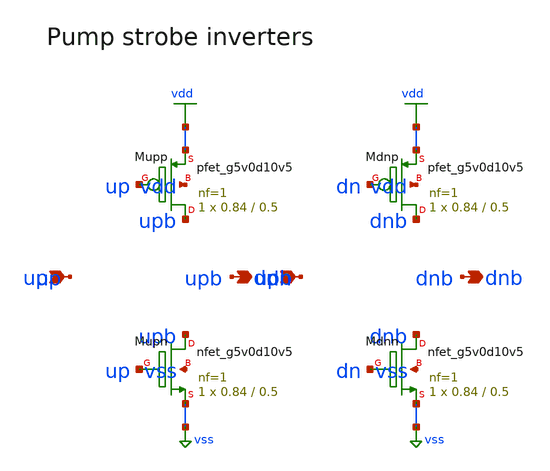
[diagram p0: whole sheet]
** sch_path: xschem/rt5w_pumpinv.sch
**.subckt rt5w_pumpinv up dn upb dnb
*.ipin up
*.ipin dn
*.opin upb
*.opin dnb
XMupp upb up vdd vdd sky130_fd_pr__pfet_g5v0d10v5 L=0.5 W=0.84 nf=1 ad=0.2436 as=0.2436 pd=2.26
+ ps=2.26 nrd=0.3452 nrs=0.3452 sa=0 sb=0 sd=0 mult=1 m=1
XMupn upb up vss vss sky130_fd_pr__nfet_g5v0d10v5 L=0.5 W=0.84 nf=1 ad=0.2436 as=0.2436 pd=2.26
+ ps=2.26 nrd=0.3452 nrs=0.3452 sa=0 sb=0 sd=0 mult=1 m=1
XMdnp dnb dn vdd vdd sky130_fd_pr__pfet_g5v0d10v5 L=0.5 W=0.84 nf=1 ad=0.2436 as=0.2436 pd=2.26
+ ps=2.26 nrd=0.3452 nrs=0.3452 sa=0 sb=0 sd=0 mult=1 m=1
XMdnn dnb dn vss vss sky130_fd_pr__nfet_g5v0d10v5 L=0.5 W=0.84 nf=1 ad=0.2436 as=0.2436 pd=2.26
+ ps=2.26 nrd=0.3452 nrs=0.3452 sa=0 sb=0 sd=0 mult=1 m=1
**.ends
.GLOBAL vdd
.GLOBAL vss
.end
